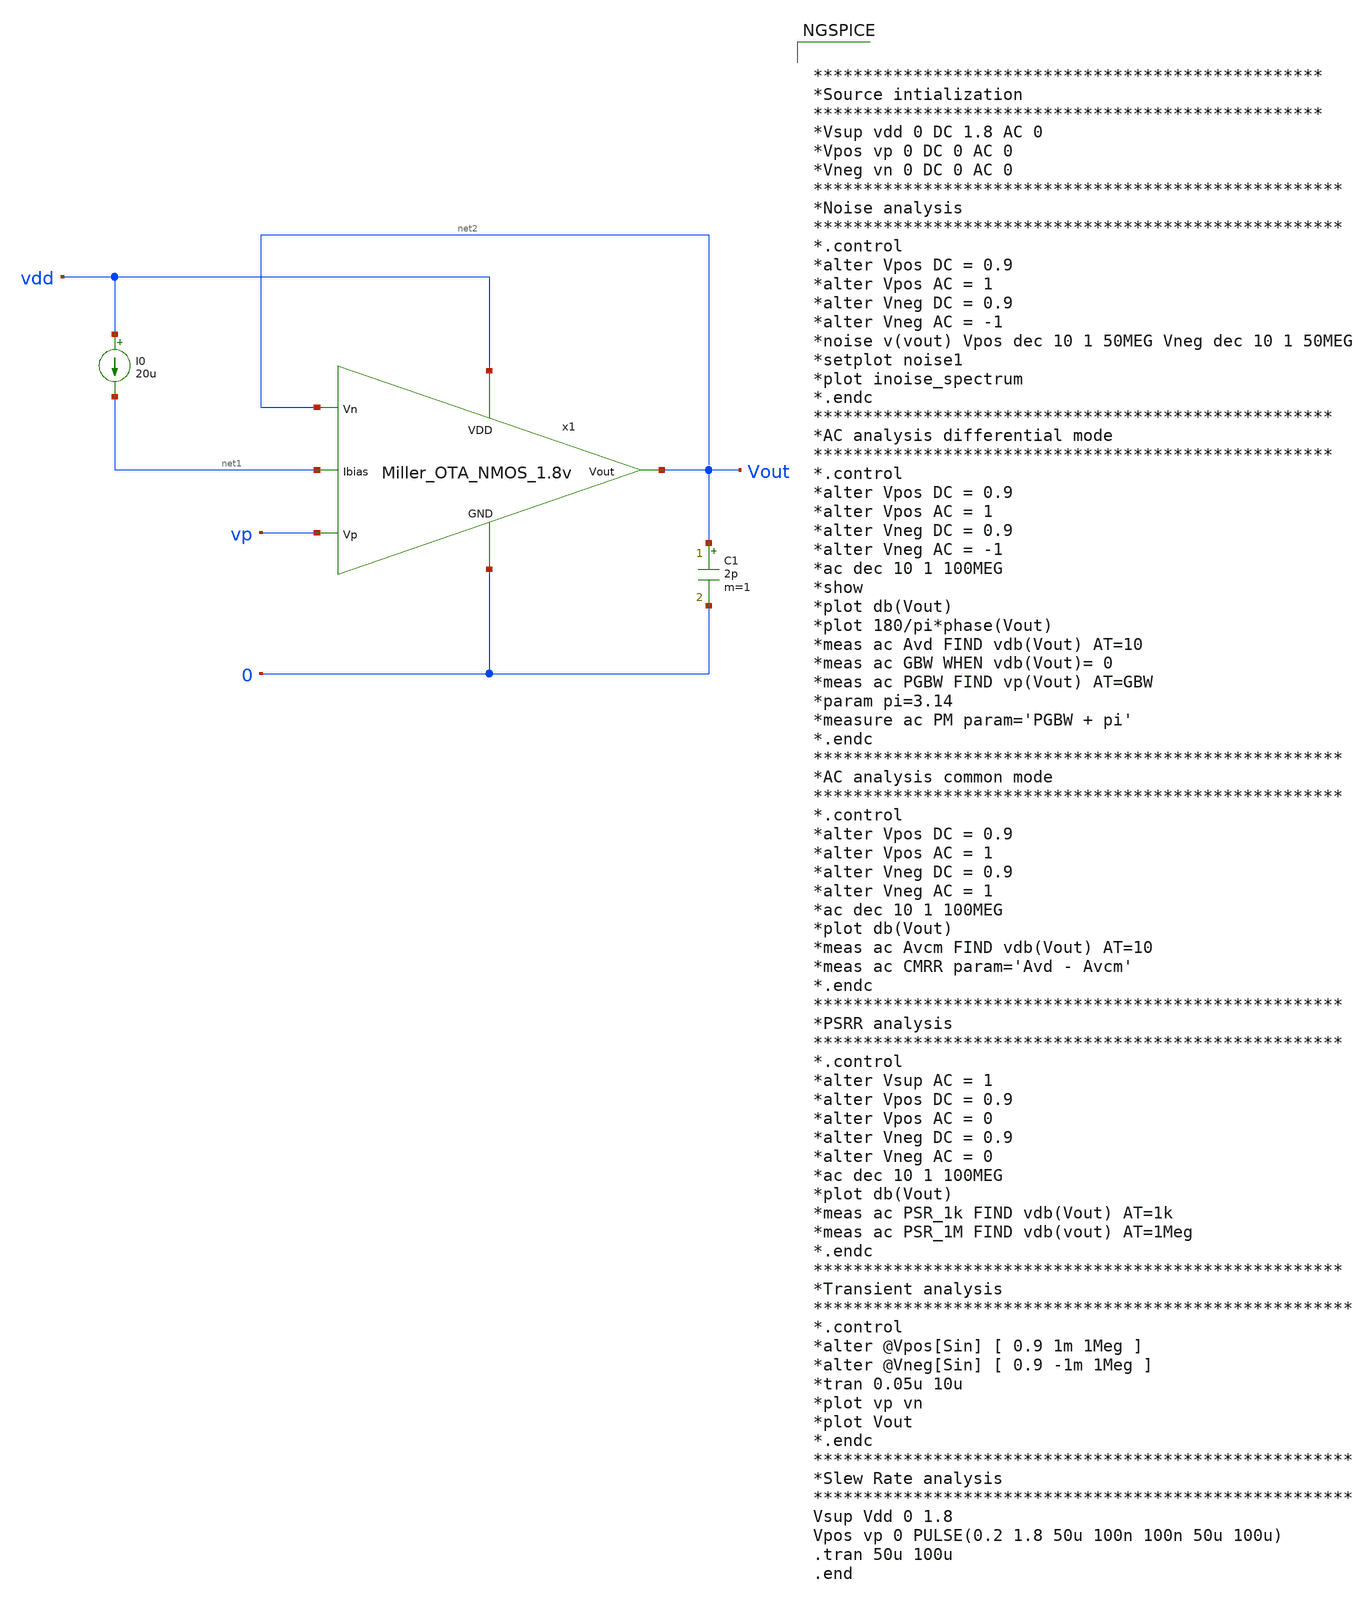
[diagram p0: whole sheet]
** sch_path: Analog_Blocks/OTA/Schematic/Miller_OTA/Transistor1.8v/Miller_OTA_meas.sch
**.subckt Miller_OTA_meas
I0 vdd net1 20u
C1 Vout 0 2p m=1
x1 vdd net2 vp Vout net1 0 Miller_OTA_NMOS_1.8v
**** begin user architecture code


***************************************************
*Source intialization
***************************************************
*Vsup vdd 0 DC 1.8 AC 0
*Vpos vp 0 DC 0 AC 0
*Vneg vn 0 DC 0 AC 0
*****************************************************
*Noise analysis
*****************************************************
*.control
*alter Vpos DC = 0.9
*alter Vpos AC = 1
*alter Vneg DC = 0.9
*alter Vneg AC = -1
*noise v(vout) Vpos dec 10 1 50MEG Vneg dec 10 1 50MEG
*setplot noise1
*plot inoise_spectrum
*.endc
****************************************************
*AC analysis differential mode
****************************************************
*.control
*alter Vpos DC = 0.9
*alter Vpos AC = 1
*alter Vneg DC = 0.9
*alter Vneg AC = -1
*ac dec 10 1 100MEG
*show
*plot db(Vout)
*plot 180/pi*phase(Vout)
*meas ac Avd FIND vdb(Vout) AT=10
*meas ac GBW WHEN vdb(Vout)= 0
*meas ac PGBW FIND vp(Vout) AT=GBW
*param pi=3.14
*measure ac PM param='PGBW + pi'
*.endc
*****************************************************
*AC analysis common mode
*****************************************************
*.control
*alter Vpos DC = 0.9
*alter Vpos AC = 1
*alter Vneg DC = 0.9
*alter Vneg AC = 1
*ac dec 10 1 100MEG
*plot db(Vout)
*meas ac Avcm FIND vdb(Vout) AT=10
*meas ac CMRR param='Avd - Avcm'
*.endc
*****************************************************
*PSRR analysis
*****************************************************
*.control
*alter Vsup AC = 1
*alter Vpos DC = 0.9
*alter Vpos AC = 0
*alter Vneg DC = 0.9
*alter Vneg AC = 0
*ac dec 10 1 100MEG
*plot db(Vout)
*meas ac PSR_1k FIND vdb(Vout) AT=1k
*meas ac PSR_1M FIND vdb(vout) AT=1Meg
*.endc
*****************************************************
*Transient analysis
******************************************************
*.control
*alter @Vpos[Sin] [ 0.9 1m 1Meg ]
*alter @Vneg[Sin] [ 0.9 -1m 1Meg ]
*tran 0.05u 10u
*plot vp vn
*plot Vout
*.endc
******************************************************
*Slew Rate analysis
******************************************************
Vsup Vdd 0 1.8
Vpos vp 0 PULSE(0.2 1.8 50u 100n 100n 50u 100u)
.tran 50u 100u
.end



.include $::SKYWATER_MODELS/cells/nfet_01v8/sky130_fd_pr__nfet_01v8__tt.corner.spice
.include $::SKYWATER_MODELS/cells/nfet_01v8_lvt/sky130_fd_pr__nfet_01v8_lvt__tt.corner.spice
.include $::SKYWATER_MODELS/cells/pfet_01v8/sky130_fd_pr__pfet_01v8__tt.corner.spice
.include $::SKYWATER_MODELS/cells/nfet_03v3_nvt/sky130_fd_pr__nfet_03v3_nvt__tt.corner.spice
.include $::SKYWATER_MODELS/cells/nfet_05v0_nvt/sky130_fd_pr__nfet_05v0_nvt__tt.corner.spice
.include $::SKYWATER_MODELS/cells/esd_nfet_01v8/sky130_fd_pr__esd_nfet_01v8__tt.corner.spice
.include $::SKYWATER_MODELS/cells/pfet_01v8_lvt/sky130_fd_pr__pfet_01v8_lvt__tt.corner.spice
.include $::SKYWATER_MODELS/cells/pfet_01v8_hvt/sky130_fd_pr__pfet_01v8_hvt__tt.corner.spice
.include $::SKYWATER_MODELS/cells/esd_pfet_g5v0d10v5/sky130_fd_pr__esd_pfet_g5v0d10v5__tt.corner.spice
.include $::SKYWATER_MODELS/cells/pfet_g5v0d10v5/sky130_fd_pr__pfet_g5v0d10v5__tt.corner.spice
.include $::SKYWATER_MODELS/cells/pfet_g5v0d16v0/sky130_fd_pr__pfet_g5v0d16v0__tt.corner.spice
.include $::SKYWATER_MODELS/cells/nfet_g5v0d10v5/sky130_fd_pr__nfet_g5v0d10v5__tt.corner.spice
.include $::SKYWATER_MODELS/cells/nfet_g5v0d16v0/sky130_fd_pr__nfet_g5v0d16v0__tt_discrete.corner.spice
.include $::SKYWATER_MODELS/cells/esd_nfet_g5v0d10v5/sky130_fd_pr__esd_nfet_g5v0d10v5__tt.corner.spice
.include $::SKYWATER_MODELS/models/corners/tt/nonfet.spice
* Mismatch parameters
.include $::SKYWATER_MODELS/cells/nfet_01v8/sky130_fd_pr__nfet_01v8__mismatch.corner.spice
.include $::SKYWATER_MODELS/cells/pfet_01v8/sky130_fd_pr__pfet_01v8__mismatch.corner.spice
.include $::SKYWATER_MODELS/cells/nfet_01v8_lvt/sky130_fd_pr__nfet_01v8_lvt__mismatch.corner.spice
.include $::SKYWATER_MODELS/cells/pfet_01v8_lvt/sky130_fd_pr__pfet_01v8_lvt__mismatch.corner.spice
.include $::SKYWATER_MODELS/cells/pfet_01v8_hvt/sky130_fd_pr__pfet_01v8_hvt__mismatch.corner.spice
.include $::SKYWATER_MODELS/cells/nfet_g5v0d10v5/sky130_fd_pr__nfet_g5v0d10v5__mismatch.corner.spice
.include $::SKYWATER_MODELS/cells/pfet_g5v0d10v5/sky130_fd_pr__pfet_g5v0d10v5__mismatch.corner.spice
.include $::SKYWATER_MODELS/cells/nfet_05v0_nvt/sky130_fd_pr__nfet_05v0_nvt__mismatch.corner.spice
.include $::SKYWATER_MODELS/cells/nfet_03v3_nvt/sky130_fd_pr__nfet_03v3_nvt__mismatch.corner.spice
* Resistor$::SKYWATER_MODELS/Capacitor
.include $::SKYWATER_MODELS/models/r+c/res_typical__cap_typical.spice
.include $::SKYWATER_MODELS/models/r+c/res_typical__cap_typical__lin.spice
* Special cells
.include $::SKYWATER_MODELS/models/corners/tt/specialized_cells.spice
* All models
.include $::SKYWATER_MODELS/models/all.spice
* Corner
.include $::SKYWATER_MODELS/models/corners/tt/rf.spice

**** end user architecture code
**.ends
.end
